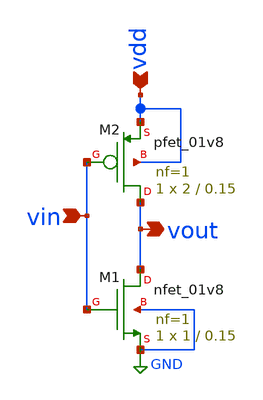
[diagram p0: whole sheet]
** sch_path: Circuit Files/Logic gate design using MOSFETS/gates/inverter_vtc.sch
**.subckt inverter_vtc vin vout vdd
*.ipin vin
*.opin vout
*.ipin vdd
XM1 vout vin GND GND sky130_fd_pr__nfet_01v8 L=0.15 W=1 nf=1 ad='int((nf+1)/2) * W/nf * 0.29' as='int((nf+2)/2) * W/nf * 0.29'
+ pd='2*int((nf+1)/2) * (W/nf + 0.29)' ps='2*int((nf+2)/2) * (W/nf + 0.29)' nrd='0.29 / W' nrs='0.29 / W'
+ sa=0 sb=0 sd=0 mult=1 m=1
XM2 vout vin vdd vdd sky130_fd_pr__pfet_01v8 L=0.15 W=2 nf=1 ad='int((nf+1)/2) * W/nf * 0.29' as='int((nf+2)/2) * W/nf * 0.29'
+ pd='2*int((nf+1)/2) * (W/nf + 0.29)' ps='2*int((nf+2)/2) * (W/nf + 0.29)' nrd='0.29 / W' nrs='0.29 / W'
+ sa=0 sb=0 sd=0 mult=1 m=1
**.ends
.GLOBAL GND
.end
